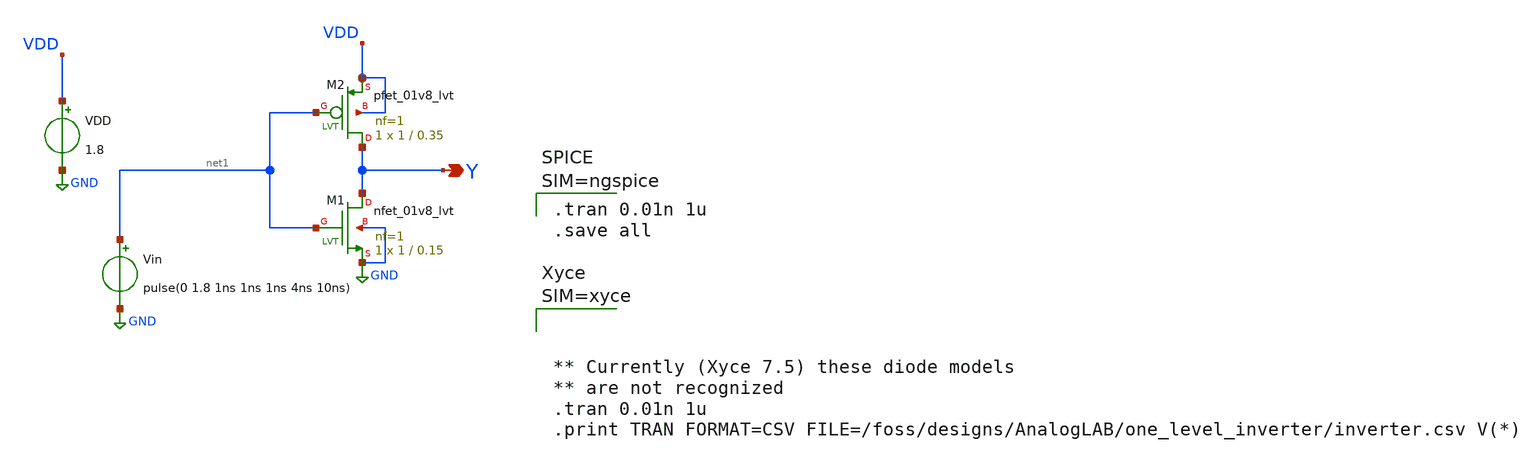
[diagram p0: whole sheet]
** sch_path: one_level_inverter/inverter.sch
**.subckt inverter Y
*.opin Y
XM1 Y net1 GND GND sky130_fd_pr__nfet_01v8_lvt L=0.15 W=1 nf=1 ad='int((nf+1)/2) * W/nf * 0.29' as='int((nf+2)/2) * W/nf * 0.29'
+ pd='2*int((nf+1)/2) * (W/nf + 0.29)' ps='2*int((nf+2)/2) * (W/nf + 0.29)' nrd='0.29 / W' nrs='0.29 / W'
+ sa=0 sb=0 sd=0 mult=1 m=1
XM2 Y net1 VDD VDD sky130_fd_pr__pfet_01v8_lvt L=0.35 W=1 nf=1 ad='int((nf+1)/2) * W/nf * 0.29' as='int((nf+2)/2) * W/nf * 0.29'
+ pd='2*int((nf+1)/2) * (W/nf + 0.29)' ps='2*int((nf+2)/2) * (W/nf + 0.29)' nrd='0.29 / W' nrs='0.29 / W'
+ sa=0 sb=0 sd=0 mult=1 m=1
VDD VDD GND 1.8
Vin net1 GND pulse(0 1.8 1ns 1ns 1ns 4ns 10ns)
**** begin user architecture code


.tran 0.01n 1u
.save all



** opencircuitdesign pdks install
.lib $::SKYWATER_MODELS/sky130.lib.spice tt





**** end user architecture code
**.ends
.GLOBAL GND
.end
